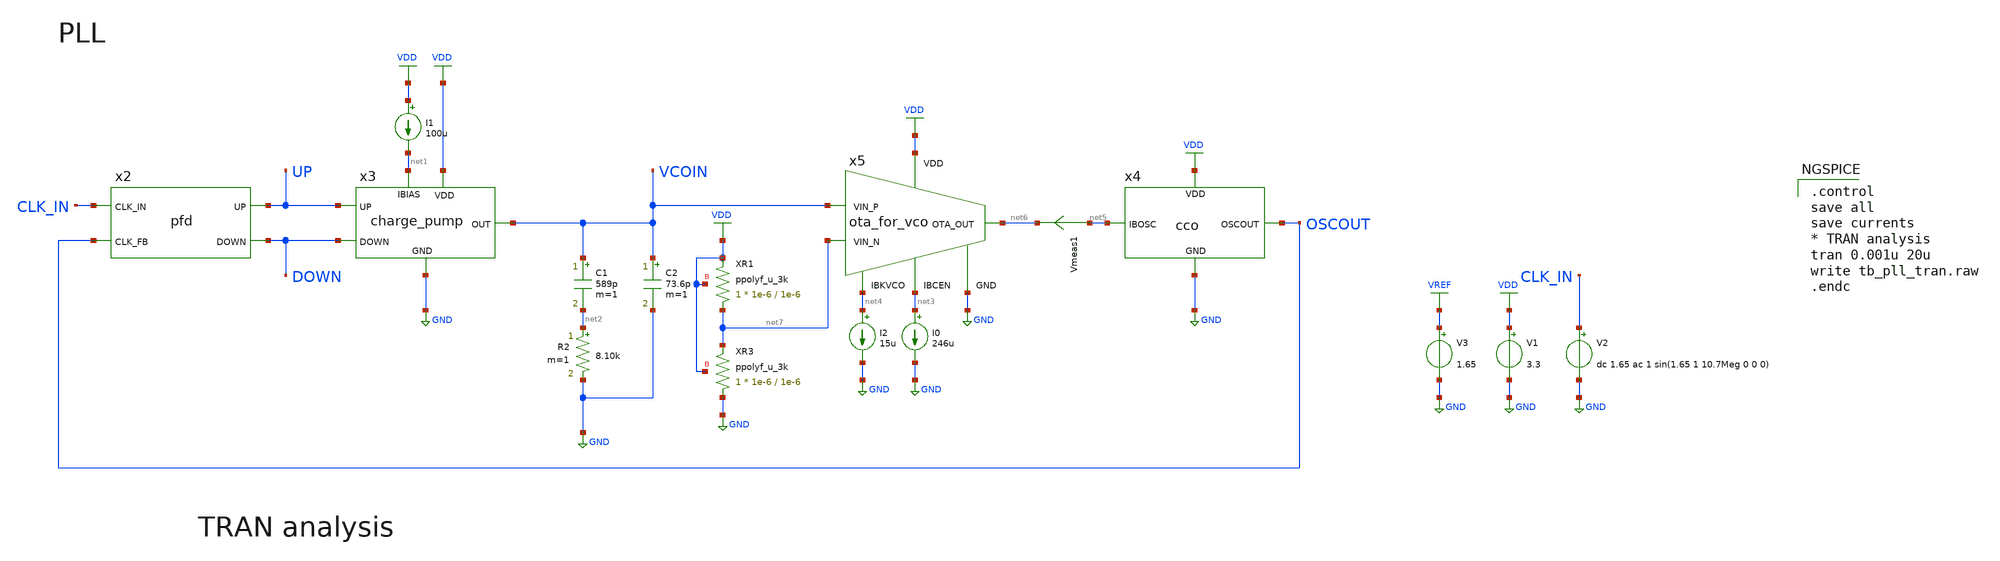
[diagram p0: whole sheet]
** sch_path: designs/libs/tb_analog/tb_pll/tb_pll.sch
* Copyright 2022 GlobalFoundries PDK Authors
* Licensed under the Apache License, Version 2.0 (the "License");
* you may not use this file except in compliance with the License.
* You may obtain a copy of the License at
* https://www.apache.org/licenses/LICENSE-2.0
* Unless required by applicable law or agreed to in writing, software
* distributed under the License is distributed on an "AS IS" BASIS,
* WITHOUT WARRANTIES OR CONDITIONS OF ANY KIND, either express or implied.
* See the License for the specific language governing permissions and
* limitations under the License.
**.subckt tb_pll
V1 VDD GND 3.3
I1 VDD net1 100u
V2 CLK_IN GND dc 1.65 ac 1 sin(1.65 1 10.7Meg 0 0 0)
V3 VREF GND 1.65
x2 UP CLK_IN OSCOUT DOWN pfd
x3 VDD GND UP DOWN VCOIN net1 charge_pump
R2 net2 GND 8.10k m=1
C1 VCOIN net2 589p m=1
C2 VCOIN GND 73.6p m=1
I0 net3 GND 246u
x4 VDD GND net5 OSCOUT cco
x5 net4 net7 VCOIN net6 GND VDD net3 ota_for_vco
I2 net4 GND 15u
Vmeas1 net5 net6 0
.save i(vmeas1)
XR1 net7 VDD VDD ppolyf_u_3k r_width=1e-6 r_length=1e-6 m=1
XR3 GND net7 VDD ppolyf_u_3k r_width=1e-6 r_length=1e-6 m=1
**** begin user architecture code

.control
save all
save currents
* TRAN analysis
tran 0.001u 20u
write tb_pll_tran.raw
.endc



.include $::180MCU_MODELS/design.ngspice
.lib $::180MCU_MODELS/sm141064.ngspice typical
.lib $::180MCU_MODELS/sm141064.ngspice cap_mim
.lib $::180MCU_MODELS/sm141064.ngspice res_typical
.lib $::180MCU_MODELS/sm141064.ngspice moscap_typical
.lib $::180MCU_MODELS/sm141064.ngspice mimcap_typical
* .lib $::180MCU_MODELS/sm141064.ngspice res_statistical
.include /foss/pdks/gf180mcuD/libs.ref/gf180mcu_fd_sc_mcu7t5v0/spice/gf180mcu_fd_sc_mcu7t5v0.spice


**** end user architecture code
**.ends
.GLOBAL VDD
.GLOBAL GND
.GLOBAL VREF
.end
